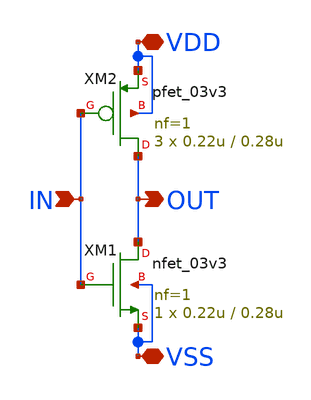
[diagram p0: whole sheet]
** sch_path: w1_advanced-foundation/w1_task/w1_inv-ring/inv1.sch
**.subckt inv1 VDD VSS IN OUT
*.iopin VDD
*.iopin VSS
*.ipin IN
*.opin OUT
XM2 OUT IN VDD VDD pfet_03v3 L=0.28u W=0.22u nf=1 ad='int((nf+1)/2) * W/nf * 0.18u' as='int((nf+2)/2) * W/nf * 0.18u'
+ pd='2*int((nf+1)/2) * (W/nf + 0.18u)' ps='2*int((nf+2)/2) * (W/nf + 0.18u)' nrd='0.18u / W' nrs='0.18u / W'
+ sa=0 sb=0 sd=0 m=3
XM1 OUT IN VSS VSS nfet_03v3 L=0.28u W=0.22u nf=1 ad='int((nf+1)/2) * W/nf * 0.18u' as='int((nf+2)/2) * W/nf * 0.18u'
+ pd='2*int((nf+1)/2) * (W/nf + 0.18u)' ps='2*int((nf+2)/2) * (W/nf + 0.18u)' nrd='0.18u / W' nrs='0.18u / W'
+ sa=0 sb=0 sd=0 m=1
**.ends
.end
